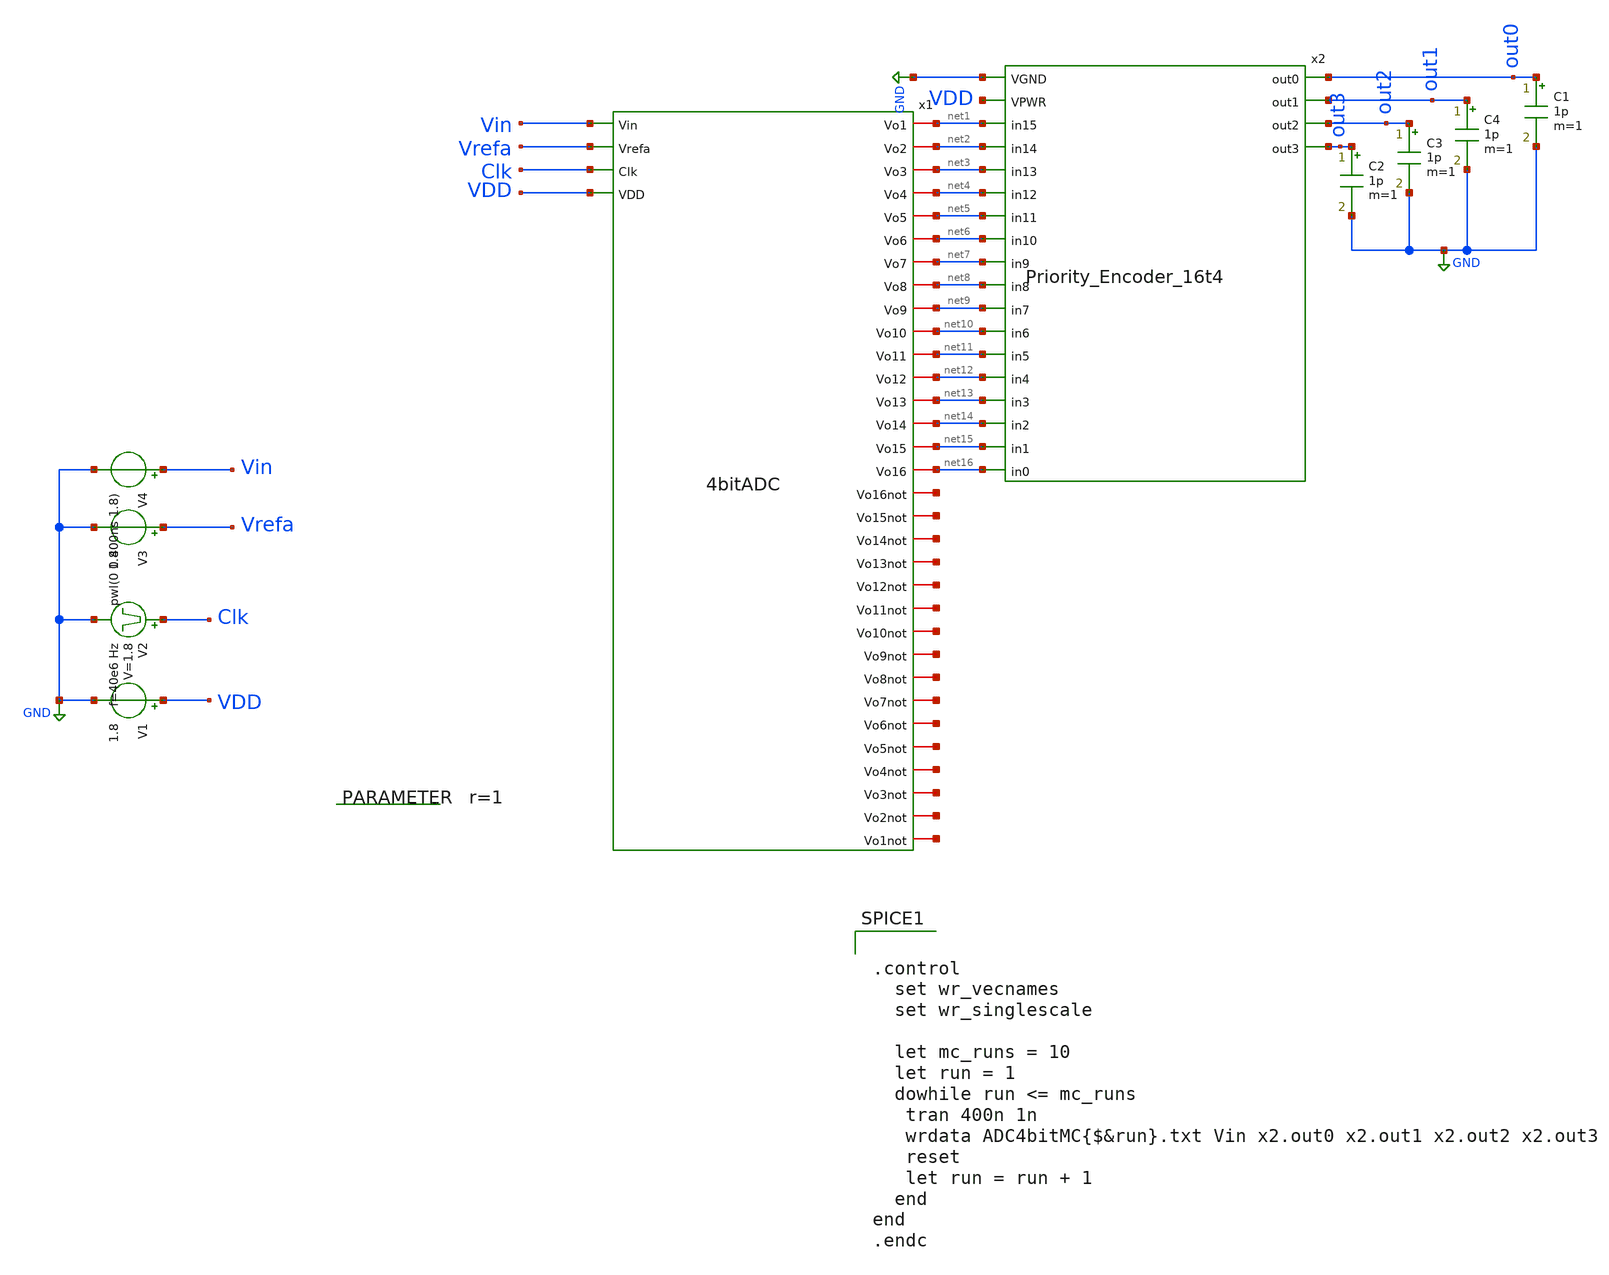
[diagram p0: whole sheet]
** sch_path: userLib/4bitADCtbMC.sch
**.subckt 4bitADCtbMC
V1 VDD GND 1.8
V3 Vrefa GND 1.8
.save i(v3)
V4 Vin GND pwl(0 0 400ns 1.8)
.param r=1
V2 Clk GND pulse 0 1.8 '0.495/ 40e6 ' '0.01/40e6 ' '0.01/40e6 ' '0.49/40e6 ' '1/40e6 '
x2 GND VDD net16 net15 net6 net5 net4 net3 net2 net1 net14 net13 net12 net11 net10 net9 net8 net7
+ out0 out1 out2 out3 Priority_Encoder_16t4
x1 net1 net2 Vin net3 Vrefa net4 net5 Clk net6 net7 VDD net8 net9 net10 net11 net12 net13 net14
+ net15 net16 net17 net18 net19 net20 net21 net22 net23 net24 net25 net26 net27 net28 net29 net30 net31
+ net32 4bitADC
C1 out0 GND 1p m=1
C2 out3 GND 1p m=1
C3 out2 GND 1p m=1
C4 out1 GND 1p m=1
**** begin user architecture code


.control
  set wr_vecnames
  set wr_singlescale

  let mc_runs = 10
  let run = 1
  dowhile run <= mc_runs
   tran 400n 1n
   wrdata ADC4bitMC{$&run}.txt Vin x2.out0 x2.out1 x2.out2 x2.out3
   reset
   let run = run + 1
  end
end
.endc



** opencircuitdesign pdks install
.include $::SKYWATER_STDCELLS/sky130_fd_sc_hd.spice


 .option wnflag=1
** opencircuitdesign pdks install
.param MC_SWITCH=1.0
.lib $::SKYWATER_MODELS/sky130.lib.spice tt


**** end user architecture code
**.ends
.GLOBAL GND
.end
